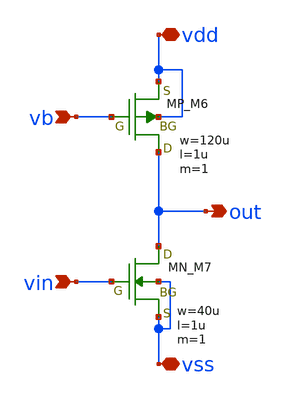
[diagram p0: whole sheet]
** sch_path: member_project/opamp/sable/mycs.sch
**.subckt mycs vb vin out vss vdd
*.ipin vb
*.ipin vin
*.opin out
*.iopin vss
*.iopin vdd
XM6 out vb vdd vdd PMOS w=120u l=1u as=0 ad=0 ps=0 pd=0 nrd=0 nrs=0 m=1
XM7 out vin vss vss NMOS w=40u l=1u as=0 ad=0 ps=0 pd=0 nrd=0 nrs=0 m=1
**.ends
.end
